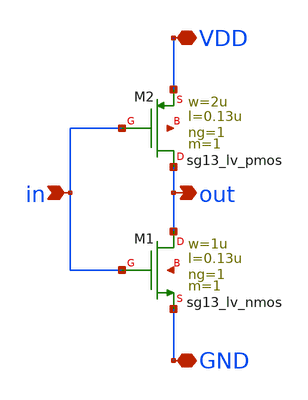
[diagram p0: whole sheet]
** sch_path: SSDOR_1V_v1/components/inv_opamp/inv.sch
**.subckt inv VDD GND in out
*.iopin VDD
*.iopin GND
*.ipin in
*.opin out
XM1 out in GND net1 sg13_lv_nmos w=1u l=0.13u ng=1 m=1 mm_ok=1
XM2 out in VDD net2 sg13_lv_pmos w=2u l=0.13u ng=1 m=1 mm_ok=1
**.ends
.end
